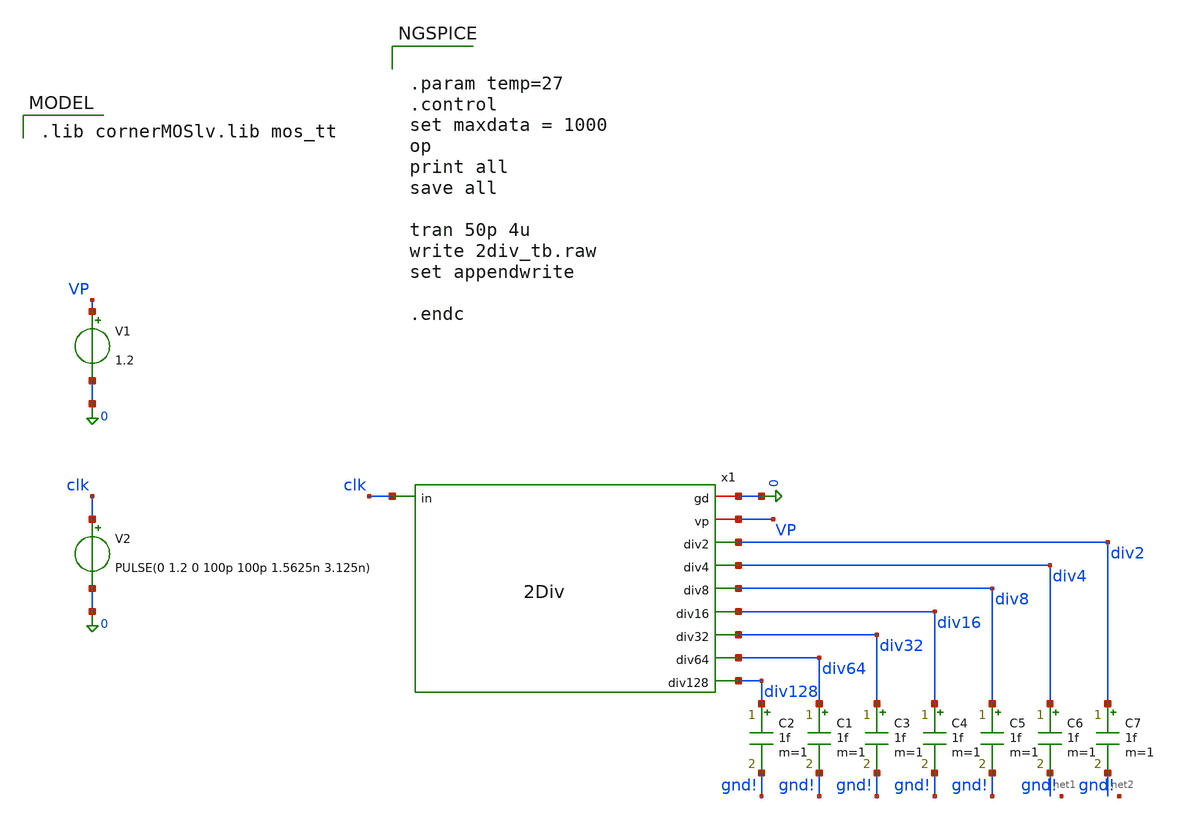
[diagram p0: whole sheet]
** sch_path: divider/tb/2Div_tb.sch
**.subckt 2Div_tb
x1 0 VP clk div2 div4 div8 div16 div32 div64 div128 2Div
V1 VP 0 1.2
V2 clk 0 PULSE(0 1.2 0 100p 100p 1.5625n 3.125n)
C2 div128 gnd! 1f m=1
C1 div64 gnd! 1f m=1
C3 div32 gnd! 1f m=1
C4 div16 gnd! 1f m=1
C5 div8 gnd! 1f m=1
C6 div4 net1 1f m=1
C7 div2 net2 1f m=1
**** begin user architecture code
 .lib cornerMOSlv.lib mos_tt



.param temp=27
.control
set maxdata = 1000
op
print all
save all

tran 50p 4u
write 2div_tb.raw
set appendwrite

.endc


**** end user architecture code
**.ends
.end
